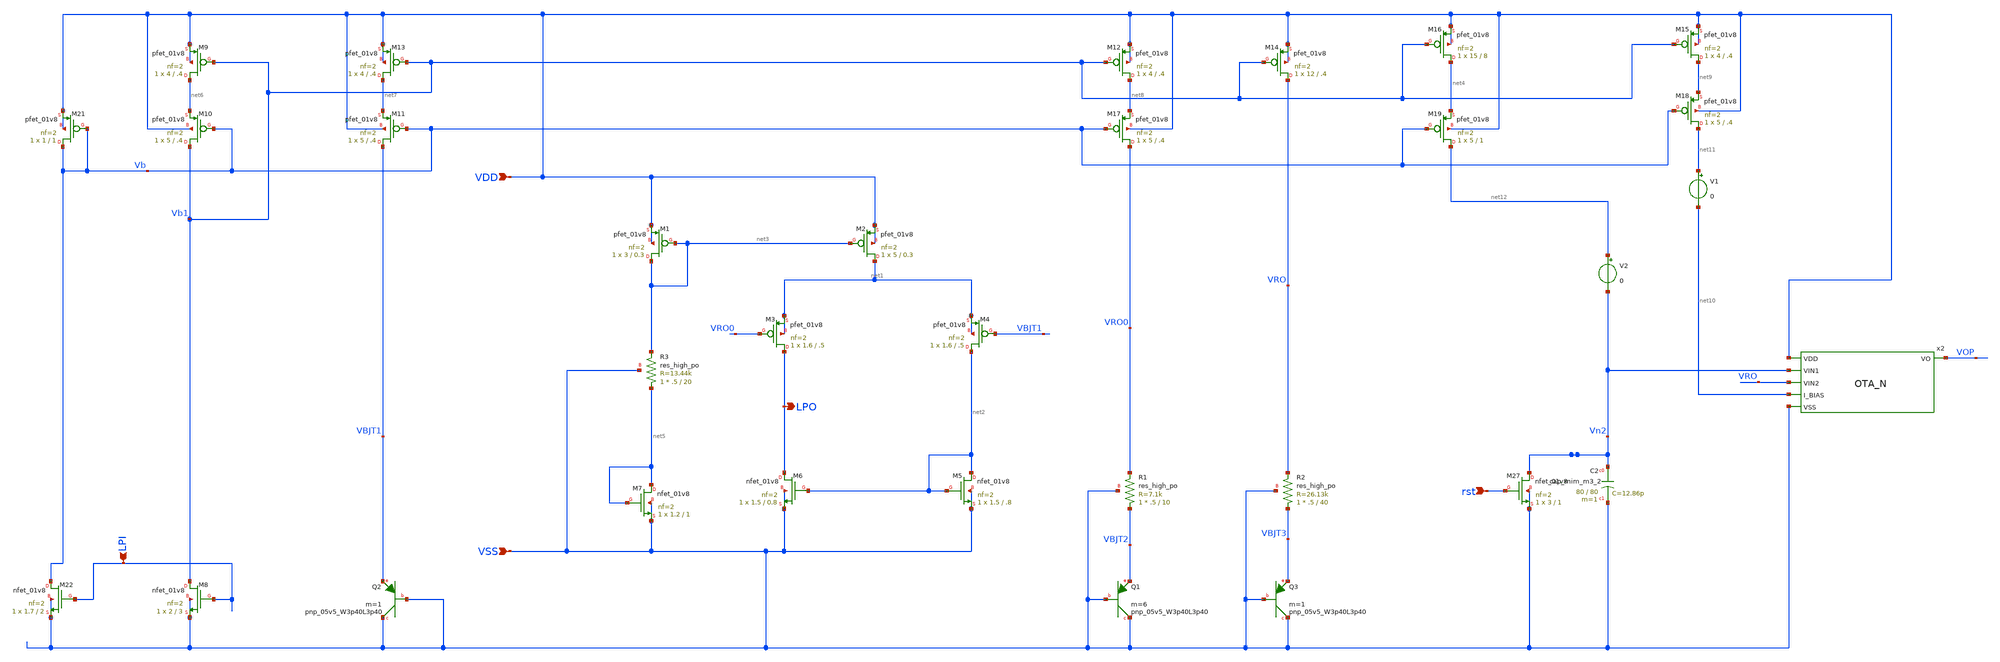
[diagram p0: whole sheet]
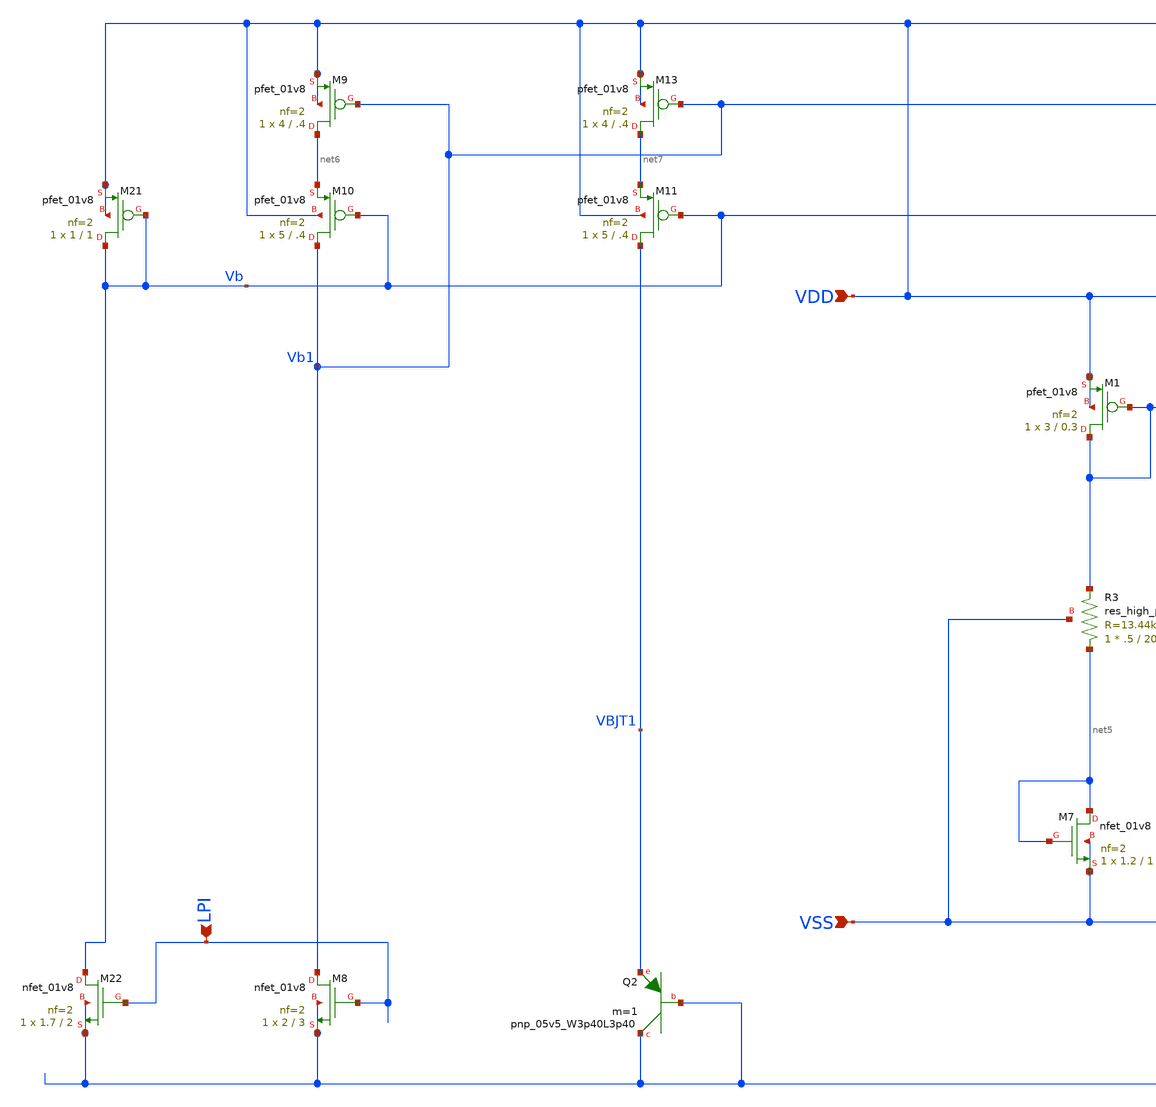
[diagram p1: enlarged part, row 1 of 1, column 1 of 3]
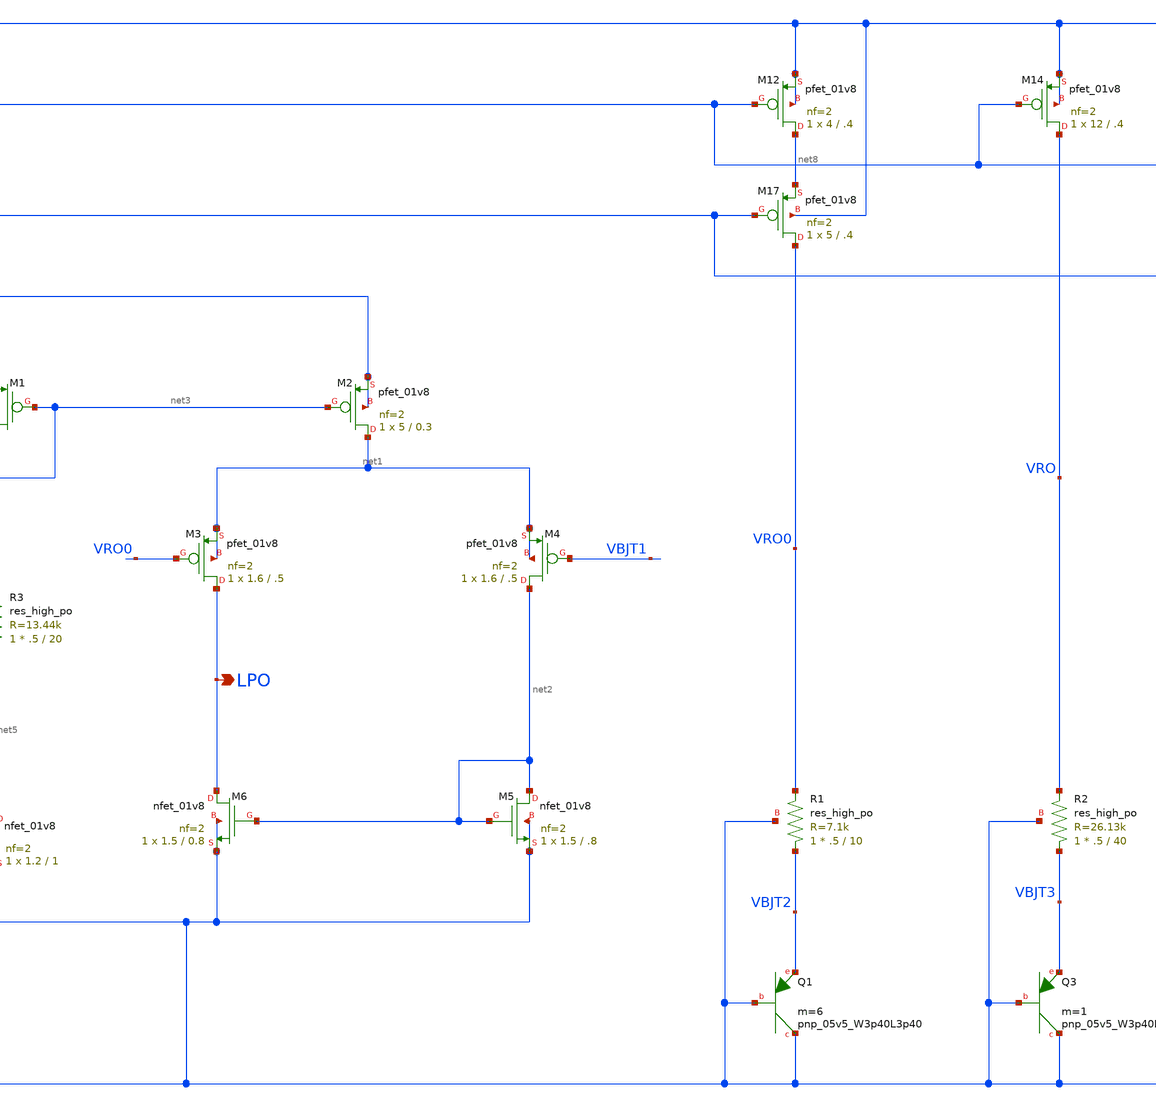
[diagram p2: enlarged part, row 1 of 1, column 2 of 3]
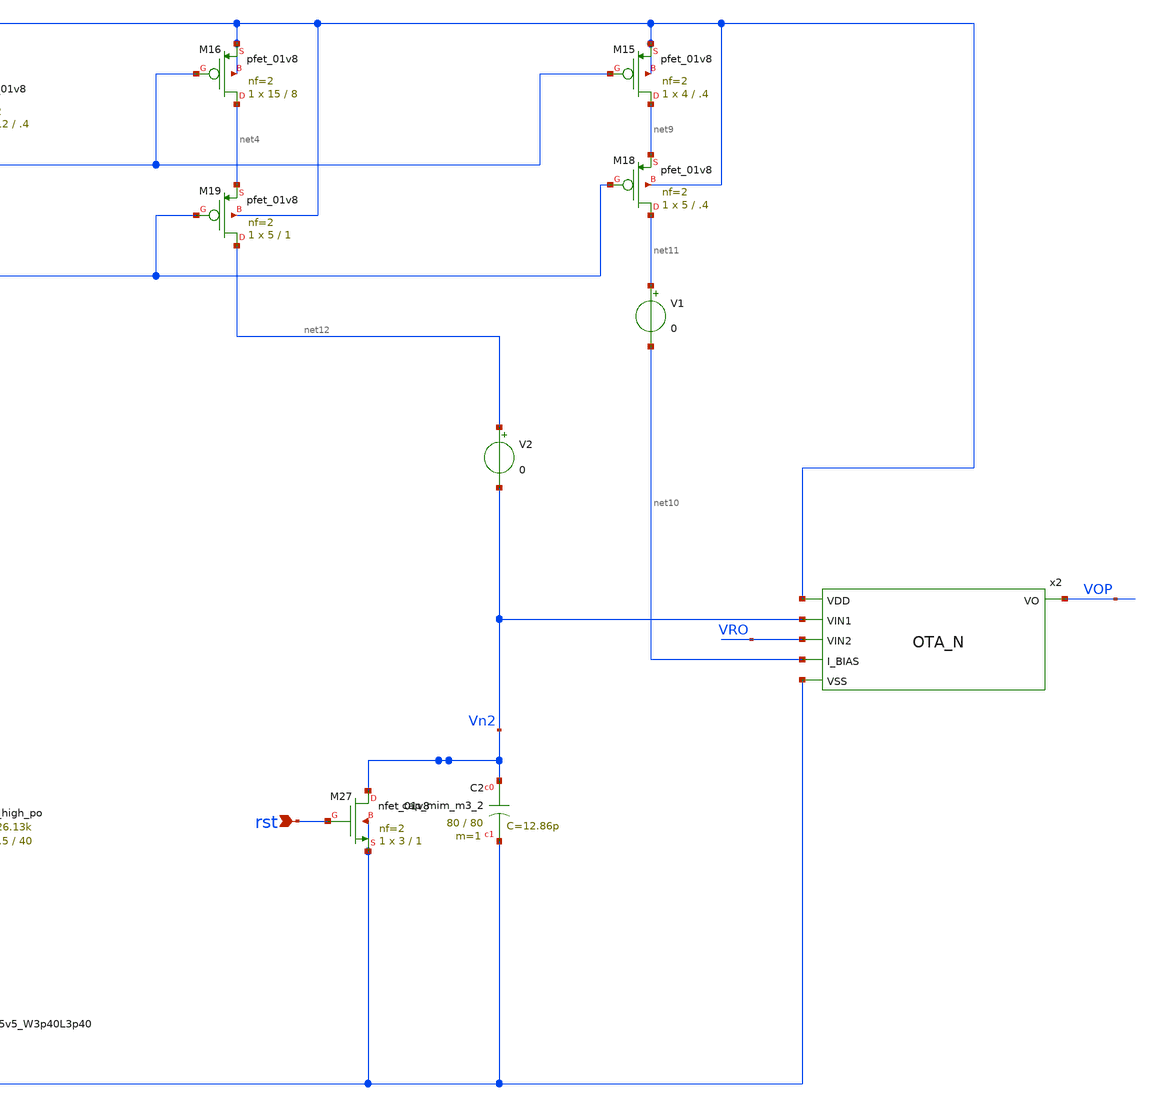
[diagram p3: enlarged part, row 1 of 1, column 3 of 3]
** sch_path: design/RPLY_EX0_SKY130NM/RPLY_EX0.sch
**.subckt RPLY_EX0 VDD VSS rst LPO LPI
*.ipin VDD
*.ipin VSS
*.ipin rst
*.opin LPO
*.ipin LPI
XQ1 VSS VSS VBJT2 sky130_fd_pr__pnp_05v5_W3p40L3p40 m=6
XQ2 VSS VSS VBJT1 sky130_fd_pr__pnp_05v5_W3p40L3p40 m=1
XM12 net8 Vb1 VDD VDD sky130_fd_pr__pfet_01v8 L=.4 W=4 nf=2 ad='int((nf+1)/2) * W/nf * 0.29' as='int((nf+2)/2) * W/nf * 0.29'
+ pd='2*int((nf+1)/2) * (W/nf + 0.29)' ps='2*int((nf+2)/2) * (W/nf + 0.29)' nrd='0.29 / W' nrs='0.29 / W'
+ sa=0 sb=0 sd=0 mult=1 m=1
XM13 net7 Vb1 VDD VDD sky130_fd_pr__pfet_01v8 L=.4 W=4 nf=2 ad='int((nf+1)/2) * W/nf * 0.29' as='int((nf+2)/2) * W/nf * 0.29'
+ pd='2*int((nf+1)/2) * (W/nf + 0.29)' ps='2*int((nf+2)/2) * (W/nf + 0.29)' nrd='0.29 / W' nrs='0.29 / W'
+ sa=0 sb=0 sd=0 mult=1 m=1
XM14 VRO Vb1 VDD VDD sky130_fd_pr__pfet_01v8 L=.4 W=12 nf=2 ad='int((nf+1)/2) * W/nf * 0.29' as='int((nf+2)/2) * W/nf * 0.29'
+ pd='2*int((nf+1)/2) * (W/nf + 0.29)' ps='2*int((nf+2)/2) * (W/nf + 0.29)' nrd='0.29 / W' nrs='0.29 / W'
+ sa=0 sb=0 sd=0 mult=1 m=1
XQ3 VSS VSS VBJT3 sky130_fd_pr__pnp_05v5_W3p40L3p40 m=1
XM16 net4 Vb1 VDD VDD sky130_fd_pr__pfet_01v8 L=8 W=15 nf=2 ad='int((nf+1)/2) * W/nf * 0.29' as='int((nf+2)/2) * W/nf * 0.29'
+ pd='2*int((nf+1)/2) * (W/nf + 0.29)' ps='2*int((nf+2)/2) * (W/nf + 0.29)' nrd='0.29 / W' nrs='0.29 / W'
+ sa=0 sb=0 sd=0 mult=1 m=1
XM1 net3 net3 VDD VDD sky130_fd_pr__pfet_01v8 L=0.3 W=3 nf=2 ad='int((nf+1)/2) * W/nf * 0.29' as='int((nf+2)/2) * W/nf * 0.29'
+ pd='2*int((nf+1)/2) * (W/nf + 0.29)' ps='2*int((nf+2)/2) * (W/nf + 0.29)' nrd='0.29 / W' nrs='0.29 / W'
+ sa=0 sb=0 sd=0 mult=1 m=1
XM2 net1 net3 VDD VDD sky130_fd_pr__pfet_01v8 L=0.3 W=5 nf=2 ad='int((nf+1)/2) * W/nf * 0.29' as='int((nf+2)/2) * W/nf * 0.29'
+ pd='2*int((nf+1)/2) * (W/nf + 0.29)' ps='2*int((nf+2)/2) * (W/nf + 0.29)' nrd='0.29 / W' nrs='0.29 / W'
+ sa=0 sb=0 sd=0 mult=1 m=1
XM3 LPO VRO0 net1 net1 sky130_fd_pr__pfet_01v8 L=.5 W=1.6 nf=2 ad='int((nf+1)/2) * W/nf * 0.29' as='int((nf+2)/2) * W/nf * 0.29'
+ pd='2*int((nf+1)/2) * (W/nf + 0.29)' ps='2*int((nf+2)/2) * (W/nf + 0.29)' nrd='0.29 / W' nrs='0.29 / W'
+ sa=0 sb=0 sd=0 mult=1 m=1
XM4 net2 VBJT1 net1 net1 sky130_fd_pr__pfet_01v8 L=.5 W=1.6 nf=2 ad='int((nf+1)/2) * W/nf * 0.29' as='int((nf+2)/2) * W/nf * 0.29'
+ pd='2*int((nf+1)/2) * (W/nf + 0.29)' ps='2*int((nf+2)/2) * (W/nf + 0.29)' nrd='0.29 / W' nrs='0.29 / W'
+ sa=0 sb=0 sd=0 mult=1 m=1
XM5 net2 net2 VSS VSS sky130_fd_pr__nfet_01v8 L=.8 W=1.5 nf=2 ad='int((nf+1)/2) * W/nf * 0.29' as='int((nf+2)/2) * W/nf * 0.29'
+ pd='2*int((nf+1)/2) * (W/nf + 0.29)' ps='2*int((nf+2)/2) * (W/nf + 0.29)' nrd='0.29 / W' nrs='0.29 / W'
+ sa=0 sb=0 sd=0 mult=1 m=1
XM6 LPO net2 VSS VSS sky130_fd_pr__nfet_01v8 L=0.8 W=1.5 nf=2 ad='int((nf+1)/2) * W/nf * 0.29' as='int((nf+2)/2) * W/nf * 0.29'
+ pd='2*int((nf+1)/2) * (W/nf + 0.29)' ps='2*int((nf+2)/2) * (W/nf + 0.29)' nrd='0.29 / W' nrs='0.29 / W'
+ sa=0 sb=0 sd=0 mult=1 m=1
XR2 VBJT3 VRO VSS sky130_fd_pr__res_high_po W=.5 L=40 mult=1 m=1
XR1 VBJT2 VRO0 VSS sky130_fd_pr__res_high_po W=.5 L=10 mult=1 m=1
XM7 net5 net5 VSS VSS sky130_fd_pr__nfet_01v8 L=1 W=1.2 nf=2 ad='int((nf+1)/2) * W/nf * 0.29' as='int((nf+2)/2) * W/nf * 0.29'
+ pd='2*int((nf+1)/2) * (W/nf + 0.29)' ps='2*int((nf+2)/2) * (W/nf + 0.29)' nrd='0.29 / W' nrs='0.29 / W'
+ sa=0 sb=0 sd=0 mult=1 m=1
XR3 net5 net3 VSS sky130_fd_pr__res_high_po W=.5 L=20 mult=1 m=1
XM8 Vb1 LPI VSS VSS sky130_fd_pr__nfet_01v8 L=3 W=2 nf=2 ad='int((nf+1)/2) * W/nf * 0.29' as='int((nf+2)/2) * W/nf * 0.29'
+ pd='2*int((nf+1)/2) * (W/nf + 0.29)' ps='2*int((nf+2)/2) * (W/nf + 0.29)' nrd='0.29 / W' nrs='0.29 / W'
+ sa=0 sb=0 sd=0 mult=1 m=1
XM9 net6 Vb1 VDD VDD sky130_fd_pr__pfet_01v8 L=.4 W=4 nf=2 ad='int((nf+1)/2) * W/nf * 0.29' as='int((nf+2)/2) * W/nf * 0.29'
+ pd='2*int((nf+1)/2) * (W/nf + 0.29)' ps='2*int((nf+2)/2) * (W/nf + 0.29)' nrd='0.29 / W' nrs='0.29 / W'
+ sa=0 sb=0 sd=0 mult=1 m=1
XM10 Vb1 Vb net6 VDD sky130_fd_pr__pfet_01v8 L=.4 W=5 nf=2 ad='int((nf+1)/2) * W/nf * 0.29' as='int((nf+2)/2) * W/nf * 0.29'
+ pd='2*int((nf+1)/2) * (W/nf + 0.29)' ps='2*int((nf+2)/2) * (W/nf + 0.29)' nrd='0.29 / W' nrs='0.29 / W'
+ sa=0 sb=0 sd=0 mult=1 m=1
XM11 VBJT1 Vb net7 VDD sky130_fd_pr__pfet_01v8 L=.4 W=5 nf=2 ad='int((nf+1)/2) * W/nf * 0.29' as='int((nf+2)/2) * W/nf * 0.29'
+ pd='2*int((nf+1)/2) * (W/nf + 0.29)' ps='2*int((nf+2)/2) * (W/nf + 0.29)' nrd='0.29 / W' nrs='0.29 / W'
+ sa=0 sb=0 sd=0 mult=1 m=1
XM17 VRO0 Vb net8 VDD sky130_fd_pr__pfet_01v8 L=.4 W=5 nf=2 ad='int((nf+1)/2) * W/nf * 0.29' as='int((nf+2)/2) * W/nf * 0.29'
+ pd='2*int((nf+1)/2) * (W/nf + 0.29)' ps='2*int((nf+2)/2) * (W/nf + 0.29)' nrd='0.29 / W' nrs='0.29 / W'
+ sa=0 sb=0 sd=0 mult=1 m=1
XM21 Vb Vb VDD VDD sky130_fd_pr__pfet_01v8 L=1 W=1 nf=2 ad='int((nf+1)/2) * W/nf * 0.29' as='int((nf+2)/2) * W/nf * 0.29'
+ pd='2*int((nf+1)/2) * (W/nf + 0.29)' ps='2*int((nf+2)/2) * (W/nf + 0.29)' nrd='0.29 / W' nrs='0.29 / W'
+ sa=0 sb=0 sd=0 mult=1 m=1
XM22 Vb LPI VSS VSS sky130_fd_pr__nfet_01v8 L=2 W=1.7 nf=2 ad='int((nf+1)/2) * W/nf * 0.29' as='int((nf+2)/2) * W/nf * 0.29'
+ pd='2*int((nf+1)/2) * (W/nf + 0.29)' ps='2*int((nf+2)/2) * (W/nf + 0.29)' nrd='0.29 / W' nrs='0.29 / W'
+ sa=0 sb=0 sd=0 mult=1 m=1
XM27 Vn2 rst VSS VSS sky130_fd_pr__nfet_01v8 L=1 W=3 nf=2 ad='int((nf+1)/2) * W/nf * 0.29' as='int((nf+2)/2) * W/nf * 0.29'
+ pd='2*int((nf+1)/2) * (W/nf + 0.29)' ps='2*int((nf+2)/2) * (W/nf + 0.29)' nrd='0.29 / W' nrs='0.29 / W'
+ sa=0 sb=0 sd=0 mult=1 m=1
x2 VDD Vn2 VRO VOP net10 VSS OTA_N
XM15 net9 Vb1 VDD VDD sky130_fd_pr__pfet_01v8 L=.4 W=4 nf=2 ad='int((nf+1)/2) * W/nf * 0.29' as='int((nf+2)/2) * W/nf * 0.29'
+ pd='2*int((nf+1)/2) * (W/nf + 0.29)' ps='2*int((nf+2)/2) * (W/nf + 0.29)' nrd='0.29 / W' nrs='0.29 / W'
+ sa=0 sb=0 sd=0 mult=1 m=1
XM18 net11 Vb net9 VDD sky130_fd_pr__pfet_01v8 L=.4 W=5 nf=2 ad='int((nf+1)/2) * W/nf * 0.29' as='int((nf+2)/2) * W/nf * 0.29'
+ pd='2*int((nf+1)/2) * (W/nf + 0.29)' ps='2*int((nf+2)/2) * (W/nf + 0.29)' nrd='0.29 / W' nrs='0.29 / W'
+ sa=0 sb=0 sd=0 mult=1 m=1
V1 net11 net10 0
.save i(v1)
V2 net12 Vn2 0
.save i(v2)
XC2 Vn2 VSS sky130_fd_pr__cap_mim_m3_2 W=80 L=80 MF=1 m=1
XM19 net12 Vb net4 VDD sky130_fd_pr__pfet_01v8 L=1 W=5 nf=2 ad='int((nf+1)/2) * W/nf * 0.29' as='int((nf+2)/2) * W/nf * 0.29'
+ pd='2*int((nf+1)/2) * (W/nf + 0.29)' ps='2*int((nf+2)/2) * (W/nf + 0.29)' nrd='0.29 / W' nrs='0.29 / W'
+ sa=0 sb=0 sd=0 mult=1 m=1
**.ends
.end
